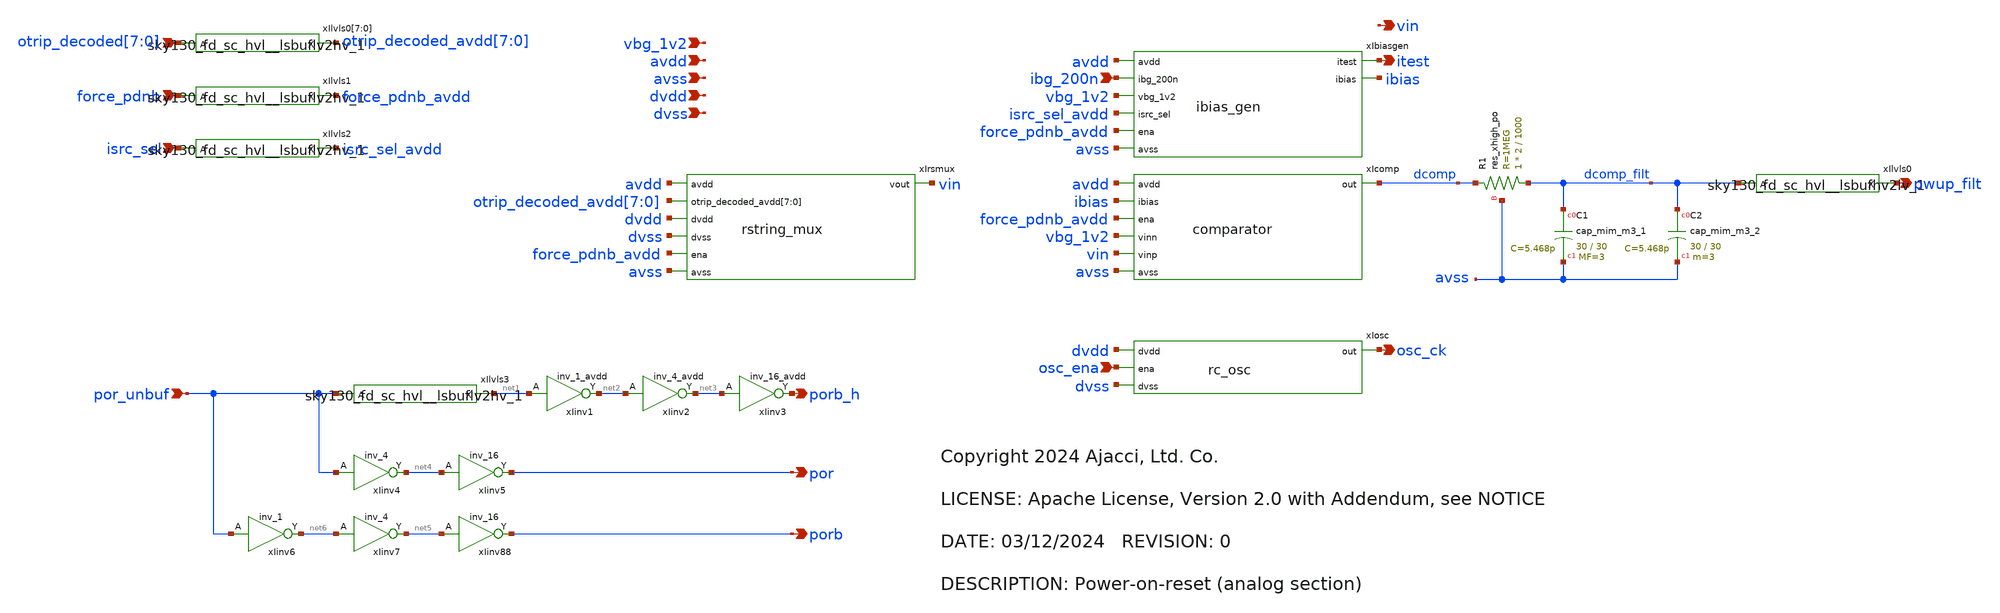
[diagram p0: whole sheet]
** sch_path: xschem/por_ana.sch
* Copyright 2024 Ajacci, Ltd. Co.
* LICENSE: Apache License, Version 2.0 with Addendum, see NOTICE
**.subckt por_ana vbg_1v2 avdd avss dvdd dvss force_pdnb isrc_sel ibg_200n pwup_filt itest osc_ena
*+ osc_ck
*+ otrip_decoded[7],otrip_decoded[6],otrip_decoded[5],otrip_decoded[4],otrip_decoded[3],otrip_decoded[2],otrip_decoded[1],otrip_decoded[0] vin por_unbuf porb_h por porb
*.ipin vbg_1v2
*.ipin avdd
*.ipin avss
*.ipin dvdd
*.ipin dvss
*.ipin force_pdnb
*.ipin isrc_sel
*.ipin ibg_200n
*.opin pwup_filt
*.opin itest
*.ipin osc_ena
*.opin osc_ck
*.ipin
*+ otrip_decoded[7],otrip_decoded[6],otrip_decoded[5],otrip_decoded[4],otrip_decoded[3],otrip_decoded[2],otrip_decoded[1],otrip_decoded[0]
*.opin vin
*.ipin por_unbuf
*.opin porb_h
*.opin por
*.opin porb
XR1 dcomp_filt dcomp avss sky130_fd_pr__res_xhigh_po W=2 L=1000 mult=1 m=1
xIlvls0 dcomp_filt dvdd avss avss avdd avdd pwup_filt sky130_fd_sc_hvl__lsbufhv2lv_1
XC1 dcomp_filt avss sky130_fd_pr__cap_mim_m3_1 W=30 L=30 MF=3 m=3
XC2 dcomp_filt avss sky130_fd_pr__cap_mim_m3_2 W=30 L=30 MF=3 m=3
xIlvls0[7] otrip_decoded[7] dvdd avss avss avdd avdd otrip_decoded_avdd[7]
+ sky130_fd_sc_hvl__lsbuflv2hv_1
xIlvls0[6] otrip_decoded[6] dvdd avss avss avdd avdd otrip_decoded_avdd[6]
+ sky130_fd_sc_hvl__lsbuflv2hv_1
xIlvls0[5] otrip_decoded[5] dvdd avss avss avdd avdd otrip_decoded_avdd[5]
+ sky130_fd_sc_hvl__lsbuflv2hv_1
xIlvls0[4] otrip_decoded[4] dvdd avss avss avdd avdd otrip_decoded_avdd[4]
+ sky130_fd_sc_hvl__lsbuflv2hv_1
xIlvls0[3] otrip_decoded[3] dvdd avss avss avdd avdd otrip_decoded_avdd[3]
+ sky130_fd_sc_hvl__lsbuflv2hv_1
xIlvls0[2] otrip_decoded[2] dvdd avss avss avdd avdd otrip_decoded_avdd[2]
+ sky130_fd_sc_hvl__lsbuflv2hv_1
xIlvls0[1] otrip_decoded[1] dvdd avss avss avdd avdd otrip_decoded_avdd[1]
+ sky130_fd_sc_hvl__lsbuflv2hv_1
xIlvls0[0] otrip_decoded[0] dvdd avss avss avdd avdd otrip_decoded_avdd[0]
+ sky130_fd_sc_hvl__lsbuflv2hv_1
xIlvls1 force_pdnb dvdd avss avss avdd avdd force_pdnb_avdd sky130_fd_sc_hvl__lsbuflv2hv_1
xIlvls2 isrc_sel dvdd avss avss avdd avdd isrc_sel_avdd sky130_fd_sc_hvl__lsbuflv2hv_1
xIrsmux avdd vin otrip_decoded_avdd[7] otrip_decoded_avdd[6] otrip_decoded_avdd[5]
+ otrip_decoded_avdd[4] otrip_decoded_avdd[3] otrip_decoded_avdd[2] otrip_decoded_avdd[1] otrip_decoded_avdd[0] dvdd dvss
+ force_pdnb_avdd avss rstring_mux
xIcomp avdd ibias dcomp force_pdnb_avdd vbg_1v2 vin avss comparator
xIbiasgen avdd itest ibias ibg_200n vbg_1v2 isrc_sel_avdd force_pdnb_avdd avss ibias_gen
xIosc dvdd osc_ck osc_ena dvss rc_osc
xIlvls3 por_unbuf dvdd avss avss avdd avdd net1 sky130_fd_sc_hvl__lsbuflv2hv_1
xIinv1 net1 avss avss avdd avdd net2 sky130_fd_sc_hvl__inv_1
xIinv2 net2 avss avss avdd avdd net3 sky130_fd_sc_hvl__inv_4
xIinv3 net3 avss avss avdd avdd porb_h sky130_fd_sc_hvl__inv_16
xIinv4 por_unbuf dvss dvss dvdd dvdd net4 sky130_fd_sc_hd__inv_4
xIinv5 net4 dvss dvss dvdd dvdd por sky130_fd_sc_hd__inv_16
xIinv7 net6 dvss dvss dvdd dvdd net5 sky130_fd_sc_hd__inv_4
xIinv88 net5 dvss dvss dvdd dvdd porb sky130_fd_sc_hd__inv_16
xIinv6 por_unbuf dvss dvss dvdd dvdd net6 sky130_fd_sc_hd__inv_1
**.ends
.end
